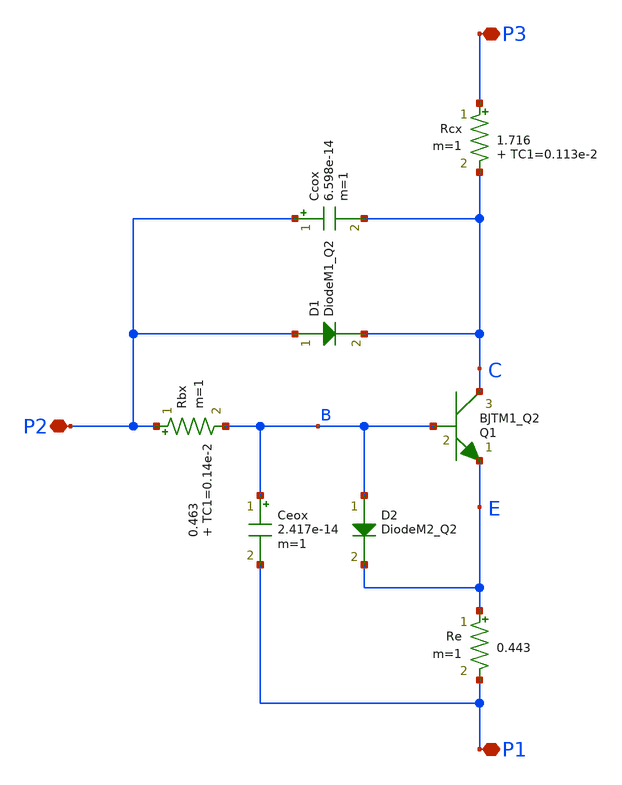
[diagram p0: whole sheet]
** sch_path: xschem_libs_newsym/examples/Q2/schematic/Q2.sch
* Copyright (C) 1998-2024 Stefan Frederik Schippers
* This program is free software; you can redistribute it and/or modify
* it under the terms of the GNU General Public License as published by
* the Free Software Foundation; either version 2 of the License, or
* (at your option) any later version.
* This program is distributed in the hope that it will be useful,
* but WITHOUT ANY WARRANTY; without even the implied warranty of
* MERCHANTABILITY or FITNESS FOR A PARTICULAR PURPOSE.  See the
* GNU General Public License for more details.
* You should have received a copy of the GNU General Public License
* along with this program; if not, write to the Free Software
**.subckt Q2 P3 P1 P2
*.iopin P3
*.iopin P1
*.iopin P2
Rcx P3 C 1.716 TC1=0.113e-2 m=1
Re E P1 0.443 m=1
Rbx P2 B 0.463 TC1=0.14e-2 m=1
Q1 C B E BJTM1_Q2 area=4 m=1
D1 P2 C DiodeM1_Q2 area=1
Ccox P2 C 6.598e-14 m=1
Ceox B P1 2.417e-14 m=1
D2 B E DiodeM2_Q2 area=1
**** begin user architecture code

* This is the BJT model used in the Agilent MSA-26 model
* documented in 5980-2496E.pdf.
* Model entered 3.30.2003 by SDB
.model BJTM1_Q2   NPN(Bf=1e6 IKF=5.895e-1 ISE=2.838e-19 NE=1.006   VAF=44 NF=1 TF=5.37e-12 XTF=20
+ VTF=0.8 ITF=8.872e-1 PTF=22   XTB=0.7 BR=1 IKR=4.4e-2 NC=2 VAR=3.37 NR=1.005 TR=4e-9   EG=1.17 IS=1.79e-17
+ XTI=3 TNOM=21 CJC=3.717e-14   VJC=0.6775 MJC=0.3319 XCJC=4.398e-1 FC=0.8 CJE=3.217e-13    VJE=0.9907
+ MJE=0.5063 RB=2.325 IRB=3.272e-4 RBM=2.5e-2 KF=1.026e-24)

* This is a diode model used in the Agilent MSA-26 model
* documented in 5980-2496E.pdf.
* Model entered 3.30.2003 by SDB
.model DIODEM1_Q2   D(IS=5.62e-17 N=1 CJO=9.676e-14    VJ=0.729 M=0.44 FC=0.8 TNOM=21)

* This is a diode model used in the Agilent MSA-26 model
* documented in 5980-2496E.pdf.
* Model entered 3.30.2003 by SDB
.model DIODEM2_Q2   D(IS=1e-24 N=1.0029 CJO=9.023e-14    VJ=0.8971 M=2.292e-1 FC=0.8 TNOM=21)



**** end user architecture code
**.ends
.end
